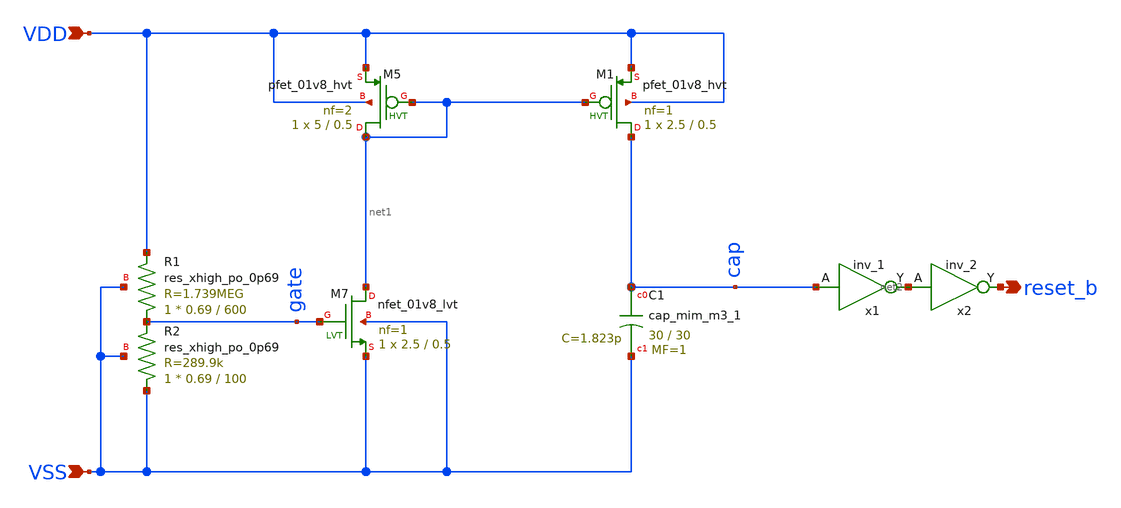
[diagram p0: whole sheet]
** sch_path: xschem/single_stage_por.sch
**.subckt single_stage_por VDD VSS reset_b
*.ipin VDD
*.ipin VSS
*.opin reset_b
XM5 net1 net1 VDD VDD sky130_fd_pr__pfet_01v8_hvt L=0.5 W=5 nf=2 ad='int((nf+1)/2) * W/nf * 0.29' as='int((nf+2)/2) * W/nf * 0.29'
+ pd='2*int((nf+1)/2) * (W/nf + 0.29)' ps='2*int((nf+2)/2) * (W/nf + 0.29)' nrd='0.29 / W' nrs='0.29 / W'
+ sa=0 sb=0 sd=0 mult=1 m=1
XM7 net1 gate VSS VSS sky130_fd_pr__nfet_01v8_lvt L=0.5 W=2.5 nf=1 ad='int((nf+1)/2) * W/nf * 0.29' as='int((nf+2)/2) * W/nf * 0.29'
+ pd='2*int((nf+1)/2) * (W/nf + 0.29)' ps='2*int((nf+2)/2) * (W/nf + 0.29)' nrd='0.29 / W' nrs='0.29 / W'
+ sa=0 sb=0 sd=0 mult=1 m=1
XR1 gate VDD VSS sky130_fd_pr__res_xhigh_po_0p69 L=600 mult=1 m=1
XR2 VSS gate VSS sky130_fd_pr__res_xhigh_po_0p69 L=100 mult=1 m=1
XM1 cap net1 VDD VDD sky130_fd_pr__pfet_01v8_hvt L=0.5 W=2.5 nf=1 ad='int((nf+1)/2) * W/nf * 0.29' as='int((nf+2)/2) * W/nf * 0.29'
+ pd='2*int((nf+1)/2) * (W/nf + 0.29)' ps='2*int((nf+2)/2) * (W/nf + 0.29)' nrd='0.29 / W' nrs='0.29 / W'
+ sa=0 sb=0 sd=0 mult=1 m=1
XC1 cap VSS sky130_fd_pr__cap_mim_m3_1 W=30 L=30 MF=1 m=1
x1 cap VSS VSS VDD VDD net2 sky130_fd_sc_hd__inv_1
x2 net2 VSS VSS VDD VDD reset_b sky130_fd_sc_hd__inv_2
**.ends
.end
